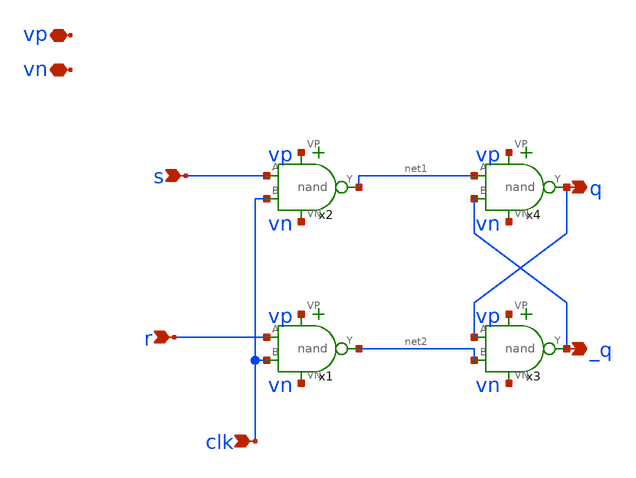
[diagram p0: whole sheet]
** sch_path: xschem/untitled-1.sch
**.subckt untitled-1 vp vn s r clk q _q
*.iopin vp
*.iopin vn
*.ipin s
*.ipin r
*.ipin clk
*.opin q
*.opin _q
x1 vn r clk net2 vp nand
x2 vn s clk net1 vp nand
x3 vn q net2 _q vp nand
x4 vn net1 _q q vp nand
**.ends

* expanding   symbol:  /home/madvlsi/dev/git/magic-dds/xschem/logic_gates/nand.sym # of pins=5
** sym_path: xschem/logic_gates/nand.sym
** sch_path: xschem/logic_gates/nand.sch
.subckt nand VN A B Y VP
*.iopin VP
*.iopin VN
*.ipin A
*.ipin B
*.opin Y
XM1 Y A net1 GND sky130_fd_pr__nfet_01v8 L=0.15 W=1 nf=1 ad='int((nf+1)/2) * W/nf * 0.29' as='int((nf+2)/2) * W/nf * 0.29'
+ pd='2*int((nf+1)/2) * (W/nf + 0.29)' ps='2*int((nf+2)/2) * (W/nf + 0.29)' nrd='0.29 / W' nrs='0.29 / W'
+ sa=0 sb=0 sd=0 mult=1 m=1
XM2 net1 B VN GND sky130_fd_pr__nfet_01v8 L=0.15 W=1 nf=1 ad='int((nf+1)/2) * W/nf * 0.29' as='int((nf+2)/2) * W/nf * 0.29'
+ pd='2*int((nf+1)/2) * (W/nf + 0.29)' ps='2*int((nf+2)/2) * (W/nf + 0.29)' nrd='0.29 / W' nrs='0.29 / W'
+ sa=0 sb=0 sd=0 mult=1 m=1
XM3 Y A VP VDD sky130_fd_pr__pfet_01v8 L=0.15 W=1 nf=1 ad='int((nf+1)/2) * W/nf * 0.29' as='int((nf+2)/2) * W/nf * 0.29'
+ pd='2*int((nf+1)/2) * (W/nf + 0.29)' ps='2*int((nf+2)/2) * (W/nf + 0.29)' nrd='0.29 / W' nrs='0.29 / W'
+ sa=0 sb=0 sd=0 mult=1 m=1
XM4 Y B VP VDD sky130_fd_pr__pfet_01v8 L=0.15 W=1 nf=1 ad='int((nf+1)/2) * W/nf * 0.29' as='int((nf+2)/2) * W/nf * 0.29'
+ pd='2*int((nf+1)/2) * (W/nf + 0.29)' ps='2*int((nf+2)/2) * (W/nf + 0.29)' nrd='0.29 / W' nrs='0.29 / W'
+ sa=0 sb=0 sd=0 mult=1 m=1
.ends

.end
